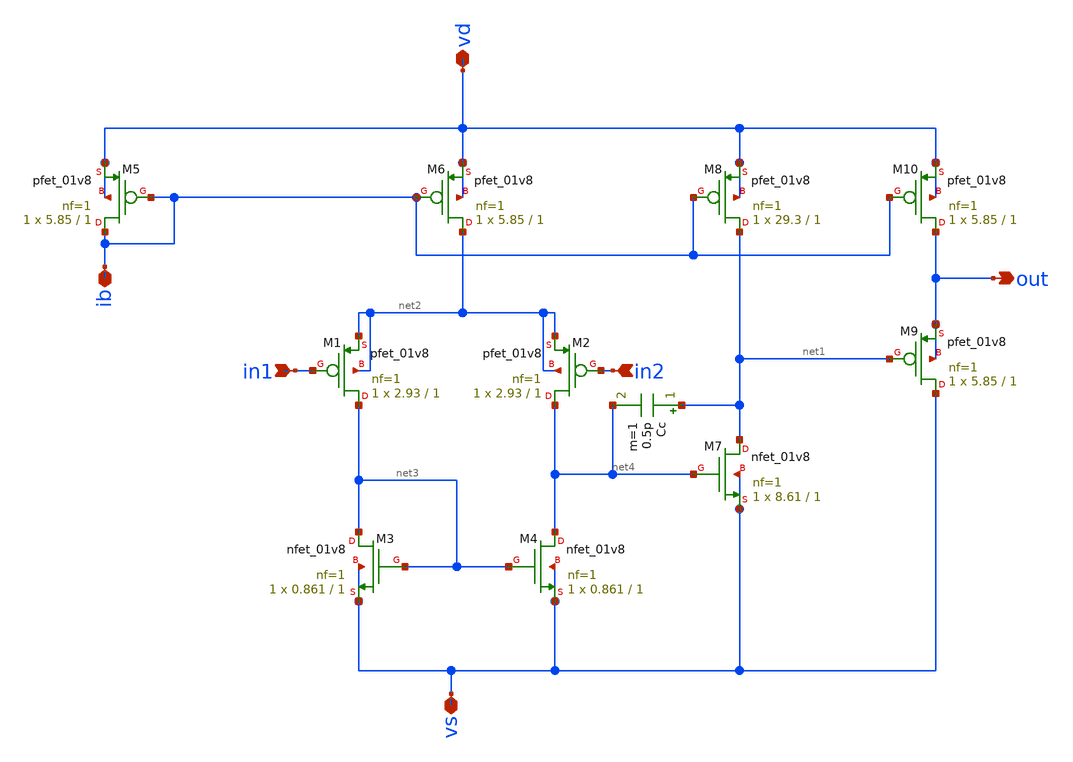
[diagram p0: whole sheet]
** sch_path: xschem/ota.sch
* Copyright 2020 Stefan Frederik Schippers
* Licensed under the Apache License, Version 2.0 (the "License");
* you may not use this file except in compliance with the License.
* You may obtain a copy of the License at
* https://www.apache.org/licenses/LICENSE-2.0
* Unless required by applicable law or agreed to in writing, software
* distributed under the License is distributed on an "AS IS" BASIS,
* WITHOUT WARRANTIES OR CONDITIONS OF ANY KIND, either express or implied.
* See the License for the specific language governing permissions and
* limitations under the License.
**.subckt ota vd out vs ib in1 in2
*.iopin vd
*.opin out
*.iopin vs
*.iopin ib
*.ipin in1
*.ipin in2
Cc net1 net4 0.5p m=1
XM4 net4 net3 vs vs sky130_fd_pr__nfet_01v8 L=1 W=0.861 nf=1 ad='int((nf+1)/2) * W/nf * 0.29' as='int((nf+2)/2) * W/nf * 0.29'
+ pd='2*int((nf+1)/2) * (W/nf + 0.29)' ps='2*int((nf+2)/2) * (W/nf + 0.29)' nrd='0.29 / W' nrs='0.29 / W'
+ sa=0 sb=0 sd=0 mult=1 m=1
XM7 net1 net4 vs vs sky130_fd_pr__nfet_01v8 L=1 W=8.61 nf=1 ad='int((nf+1)/2) * W/nf * 0.29' as='int((nf+2)/2) * W/nf * 0.29'
+ pd='2*int((nf+1)/2) * (W/nf + 0.29)' ps='2*int((nf+2)/2) * (W/nf + 0.29)' nrd='0.29 / W' nrs='0.29 / W'
+ sa=0 sb=0 sd=0 mult=1 m=1
XM5 ib ib vd vd sky130_fd_pr__pfet_01v8 L=1 W=5.85 nf=1 ad='int((nf+1)/2) * W/nf * 0.29' as='int((nf+2)/2) * W/nf * 0.29'
+ pd='2*int((nf+1)/2) * (W/nf + 0.29)' ps='2*int((nf+2)/2) * (W/nf + 0.29)' nrd='0.29 / W' nrs='0.29 / W'
+ sa=0 sb=0 sd=0 mult=1 m=1
XM6 net2 ib vd vd sky130_fd_pr__pfet_01v8 L=1 W=5.85 nf=1 ad='int((nf+1)/2) * W/nf * 0.29' as='int((nf+2)/2) * W/nf * 0.29'
+ pd='2*int((nf+1)/2) * (W/nf + 0.29)' ps='2*int((nf+2)/2) * (W/nf + 0.29)' nrd='0.29 / W' nrs='0.29 / W'
+ sa=0 sb=0 sd=0 mult=1 m=1
XM8 net1 ib vd vd sky130_fd_pr__pfet_01v8 L=1 W=29.3 nf=1 ad='int((nf+1)/2) * W/nf * 0.29' as='int((nf+2)/2) * W/nf * 0.29'
+ pd='2*int((nf+1)/2) * (W/nf + 0.29)' ps='2*int((nf+2)/2) * (W/nf + 0.29)' nrd='0.29 / W' nrs='0.29 / W'
+ sa=0 sb=0 sd=0 mult=1 m=1
XM10 out ib vd vd sky130_fd_pr__pfet_01v8 L=1 W=5.85 nf=1 ad='int((nf+1)/2) * W/nf * 0.29' as='int((nf+2)/2) * W/nf * 0.29'
+ pd='2*int((nf+1)/2) * (W/nf + 0.29)' ps='2*int((nf+2)/2) * (W/nf + 0.29)' nrd='0.29 / W' nrs='0.29 / W'
+ sa=0 sb=0 sd=0 mult=1 m=1
XM9 vs net1 out out sky130_fd_pr__pfet_01v8 L=1 W=5.85 nf=1 ad='int((nf+1)/2) * W/nf * 0.29' as='int((nf+2)/2) * W/nf * 0.29'
+ pd='2*int((nf+1)/2) * (W/nf + 0.29)' ps='2*int((nf+2)/2) * (W/nf + 0.29)' nrd='0.29 / W' nrs='0.29 / W'
+ sa=0 sb=0 sd=0 mult=1 m=1
XM1 net3 in1 net2 net2 sky130_fd_pr__pfet_01v8 L=1 W=2.93 nf=1 ad='int((nf+1)/2) * W/nf * 0.29' as='int((nf+2)/2) * W/nf * 0.29'
+ pd='2*int((nf+1)/2) * (W/nf + 0.29)' ps='2*int((nf+2)/2) * (W/nf + 0.29)' nrd='0.29 / W' nrs='0.29 / W'
+ sa=0 sb=0 sd=0 mult=1 m=1
XM2 net4 in2 net2 net2 sky130_fd_pr__pfet_01v8 L=1 W=2.93 nf=1 ad='int((nf+1)/2) * W/nf * 0.29' as='int((nf+2)/2) * W/nf * 0.29'
+ pd='2*int((nf+1)/2) * (W/nf + 0.29)' ps='2*int((nf+2)/2) * (W/nf + 0.29)' nrd='0.29 / W' nrs='0.29 / W'
+ sa=0 sb=0 sd=0 mult=1 m=1
XM3 net3 net3 vs vs sky130_fd_pr__nfet_01v8 L=1 W=0.861 nf=1 ad='int((nf+1)/2) * W/nf * 0.29' as='int((nf+2)/2) * W/nf * 0.29'
+ pd='2*int((nf+1)/2) * (W/nf + 0.29)' ps='2*int((nf+2)/2) * (W/nf + 0.29)' nrd='0.29 / W' nrs='0.29 / W'
+ sa=0 sb=0 sd=0 mult=1 m=1
**.ends
.end
